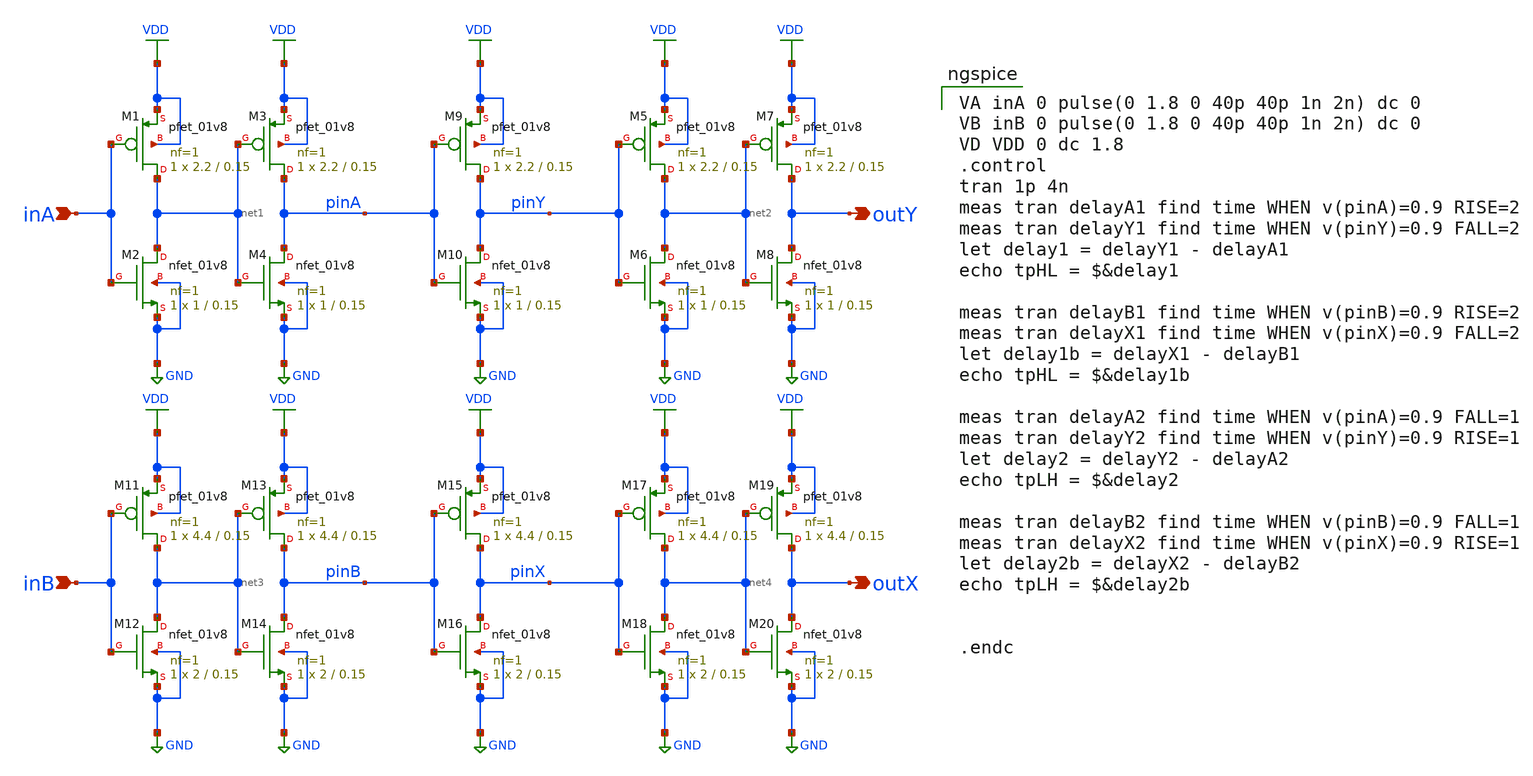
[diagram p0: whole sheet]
** sch_path: inv_delay2.sch
**.subckt inv_delay2 inA outY inB outX
*.ipin inA
*.opin outY
*.ipin inB
*.opin outX
XM1 net1 inA VDD VDD sky130_fd_pr__pfet_01v8 L=0.15 W=2.2 nf=1 ad='int((nf+1)/2) * W/nf * 0.29' as='int((nf+2)/2) * W/nf * 0.29'
+ pd='2*int((nf+1)/2) * (W/nf + 0.29)' ps='2*int((nf+2)/2) * (W/nf + 0.29)' nrd='0.29 / W' nrs='0.29 / W'
+ sa=0 sb=0 sd=0 mult=1 m=1
XM2 net1 inA GND GND sky130_fd_pr__nfet_01v8 L=0.15 W=1 nf=1 ad='int((nf+1)/2) * W/nf * 0.29' as='int((nf+2)/2) * W/nf * 0.29'
+ pd='2*int((nf+1)/2) * (W/nf + 0.29)' ps='2*int((nf+2)/2) * (W/nf + 0.29)' nrd='0.29 / W' nrs='0.29 / W'
+ sa=0 sb=0 sd=0 mult=1 m=1
XM3 pinA net1 VDD VDD sky130_fd_pr__pfet_01v8 L=0.15 W=2.2 nf=1 ad='int((nf+1)/2) * W/nf * 0.29' as='int((nf+2)/2) * W/nf * 0.29'
+ pd='2*int((nf+1)/2) * (W/nf + 0.29)' ps='2*int((nf+2)/2) * (W/nf + 0.29)' nrd='0.29 / W' nrs='0.29 / W'
+ sa=0 sb=0 sd=0 mult=1 m=1
XM4 pinA net1 GND GND sky130_fd_pr__nfet_01v8 L=0.15 W=1 nf=1 ad='int((nf+1)/2) * W/nf * 0.29' as='int((nf+2)/2) * W/nf * 0.29'
+ pd='2*int((nf+1)/2) * (W/nf + 0.29)' ps='2*int((nf+2)/2) * (W/nf + 0.29)' nrd='0.29 / W' nrs='0.29 / W'
+ sa=0 sb=0 sd=0 mult=1 m=1
XM5 net2 pinY VDD VDD sky130_fd_pr__pfet_01v8 L=0.15 W=2.2 nf=1 ad='int((nf+1)/2) * W/nf * 0.29' as='int((nf+2)/2) * W/nf * 0.29'
+ pd='2*int((nf+1)/2) * (W/nf + 0.29)' ps='2*int((nf+2)/2) * (W/nf + 0.29)' nrd='0.29 / W' nrs='0.29 / W'
+ sa=0 sb=0 sd=0 mult=1 m=1
XM6 net2 pinY GND GND sky130_fd_pr__nfet_01v8 L=0.15 W=1 nf=1 ad='int((nf+1)/2) * W/nf * 0.29' as='int((nf+2)/2) * W/nf * 0.29'
+ pd='2*int((nf+1)/2) * (W/nf + 0.29)' ps='2*int((nf+2)/2) * (W/nf + 0.29)' nrd='0.29 / W' nrs='0.29 / W'
+ sa=0 sb=0 sd=0 mult=1 m=1
XM7 outY net2 VDD VDD sky130_fd_pr__pfet_01v8 L=0.15 W=2.2 nf=1 ad='int((nf+1)/2) * W/nf * 0.29' as='int((nf+2)/2) * W/nf * 0.29'
+ pd='2*int((nf+1)/2) * (W/nf + 0.29)' ps='2*int((nf+2)/2) * (W/nf + 0.29)' nrd='0.29 / W' nrs='0.29 / W'
+ sa=0 sb=0 sd=0 mult=1 m=1
XM8 outY net2 GND GND sky130_fd_pr__nfet_01v8 L=0.15 W=1 nf=1 ad='int((nf+1)/2) * W/nf * 0.29' as='int((nf+2)/2) * W/nf * 0.29'
+ pd='2*int((nf+1)/2) * (W/nf + 0.29)' ps='2*int((nf+2)/2) * (W/nf + 0.29)' nrd='0.29 / W' nrs='0.29 / W'
+ sa=0 sb=0 sd=0 mult=1 m=1
XM9 pinY pinA VDD VDD sky130_fd_pr__pfet_01v8 L=0.15 W=2.2 nf=1 ad='int((nf+1)/2) * W/nf * 0.29' as='int((nf+2)/2) * W/nf * 0.29'
+ pd='2*int((nf+1)/2) * (W/nf + 0.29)' ps='2*int((nf+2)/2) * (W/nf + 0.29)' nrd='0.29 / W' nrs='0.29 / W'
+ sa=0 sb=0 sd=0 mult=1 m=1
XM10 pinY pinA GND GND sky130_fd_pr__nfet_01v8 L=0.15 W=1 nf=1 ad='int((nf+1)/2) * W/nf * 0.29' as='int((nf+2)/2) * W/nf * 0.29'
+ pd='2*int((nf+1)/2) * (W/nf + 0.29)' ps='2*int((nf+2)/2) * (W/nf + 0.29)' nrd='0.29 / W' nrs='0.29 / W'
+ sa=0 sb=0 sd=0 mult=1 m=1
XM11 net3 inB VDD VDD sky130_fd_pr__pfet_01v8 L=0.15 W=4.4 nf=1 ad='int((nf+1)/2) * W/nf * 0.29' as='int((nf+2)/2) * W/nf * 0.29'
+ pd='2*int((nf+1)/2) * (W/nf + 0.29)' ps='2*int((nf+2)/2) * (W/nf + 0.29)' nrd='0.29 / W' nrs='0.29 / W'
+ sa=0 sb=0 sd=0 mult=1 m=1
XM12 net3 inB GND GND sky130_fd_pr__nfet_01v8 L=0.15 W=2 nf=1 ad='int((nf+1)/2) * W/nf * 0.29' as='int((nf+2)/2) * W/nf * 0.29'
+ pd='2*int((nf+1)/2) * (W/nf + 0.29)' ps='2*int((nf+2)/2) * (W/nf + 0.29)' nrd='0.29 / W' nrs='0.29 / W'
+ sa=0 sb=0 sd=0 mult=1 m=1
XM19 outX net4 VDD VDD sky130_fd_pr__pfet_01v8 L=0.15 W=4.4 nf=1 ad='int((nf+1)/2) * W/nf * 0.29' as='int((nf+2)/2) * W/nf * 0.29'
+ pd='2*int((nf+1)/2) * (W/nf + 0.29)' ps='2*int((nf+2)/2) * (W/nf + 0.29)' nrd='0.29 / W' nrs='0.29 / W'
+ sa=0 sb=0 sd=0 mult=1 m=1
XM13 pinB net3 VDD VDD sky130_fd_pr__pfet_01v8 L=0.15 W=4.4 nf=1 ad='int((nf+1)/2) * W/nf * 0.29' as='int((nf+2)/2) * W/nf * 0.29'
+ pd='2*int((nf+1)/2) * (W/nf + 0.29)' ps='2*int((nf+2)/2) * (W/nf + 0.29)' nrd='0.29 / W' nrs='0.29 / W'
+ sa=0 sb=0 sd=0 mult=1 m=1
XM15 pinX pinB VDD VDD sky130_fd_pr__pfet_01v8 L=0.15 W=4.4 nf=1 ad='int((nf+1)/2) * W/nf * 0.29' as='int((nf+2)/2) * W/nf * 0.29'
+ pd='2*int((nf+1)/2) * (W/nf + 0.29)' ps='2*int((nf+2)/2) * (W/nf + 0.29)' nrd='0.29 / W' nrs='0.29 / W'
+ sa=0 sb=0 sd=0 mult=1 m=1
XM17 net4 pinX VDD VDD sky130_fd_pr__pfet_01v8 L=0.15 W=4.4 nf=1 ad='int((nf+1)/2) * W/nf * 0.29' as='int((nf+2)/2) * W/nf * 0.29'
+ pd='2*int((nf+1)/2) * (W/nf + 0.29)' ps='2*int((nf+2)/2) * (W/nf + 0.29)' nrd='0.29 / W' nrs='0.29 / W'
+ sa=0 sb=0 sd=0 mult=1 m=1
XM14 pinB net3 GND GND sky130_fd_pr__nfet_01v8 L=0.15 W=2 nf=1 ad='int((nf+1)/2) * W/nf * 0.29' as='int((nf+2)/2) * W/nf * 0.29'
+ pd='2*int((nf+1)/2) * (W/nf + 0.29)' ps='2*int((nf+2)/2) * (W/nf + 0.29)' nrd='0.29 / W' nrs='0.29 / W'
+ sa=0 sb=0 sd=0 mult=1 m=1
XM16 pinX pinB GND GND sky130_fd_pr__nfet_01v8 L=0.15 W=2 nf=1 ad='int((nf+1)/2) * W/nf * 0.29' as='int((nf+2)/2) * W/nf * 0.29'
+ pd='2*int((nf+1)/2) * (W/nf + 0.29)' ps='2*int((nf+2)/2) * (W/nf + 0.29)' nrd='0.29 / W' nrs='0.29 / W'
+ sa=0 sb=0 sd=0 mult=1 m=1
XM18 net4 pinX GND GND sky130_fd_pr__nfet_01v8 L=0.15 W=2 nf=1 ad='int((nf+1)/2) * W/nf * 0.29' as='int((nf+2)/2) * W/nf * 0.29'
+ pd='2*int((nf+1)/2) * (W/nf + 0.29)' ps='2*int((nf+2)/2) * (W/nf + 0.29)' nrd='0.29 / W' nrs='0.29 / W'
+ sa=0 sb=0 sd=0 mult=1 m=1
XM20 outX net4 GND GND sky130_fd_pr__nfet_01v8 L=0.15 W=2 nf=1 ad='int((nf+1)/2) * W/nf * 0.29' as='int((nf+2)/2) * W/nf * 0.29'
+ pd='2*int((nf+1)/2) * (W/nf + 0.29)' ps='2*int((nf+2)/2) * (W/nf + 0.29)' nrd='0.29 / W' nrs='0.29 / W'
+ sa=0 sb=0 sd=0 mult=1 m=1
**** begin user architecture code

VA inA 0 pulse(0 1.8 0 40p 40p 1n 2n) dc 0
VB inB 0 pulse(0 1.8 0 40p 40p 1n 2n) dc 0
VD VDD 0 dc 1.8
.control
tran 1p 4n
meas tran delayA1 find time WHEN v(pinA)=0.9 RISE=2
meas tran delayY1 find time WHEN v(pinY)=0.9 FALL=2
let delay1 = delayY1 - delayA1
echo tpHL = $&delay1

meas tran delayB1 find time WHEN v(pinB)=0.9 RISE=2
meas tran delayX1 find time WHEN v(pinX)=0.9 FALL=2
let delay1b = delayX1 - delayB1
echo tpHL = $&delay1b

meas tran delayA2 find time WHEN v(pinA)=0.9 FALL=1
meas tran delayY2 find time WHEN v(pinY)=0.9 RISE=1
let delay2 = delayY2 - delayA2
echo tpLH = $&delay2

meas tran delayB2 find time WHEN v(pinB)=0.9 FALL=1
meas tran delayX2 find time WHEN v(pinX)=0.9 RISE=1
let delay2b = delayX2 - delayB2
echo tpLH = $&delay2b


.endc

 .param mc_mm_switch=0
.param mc_pr_switch=0
.include $::SKYWATER_MODELS/corners/tt.spice
.include $::SKYWATER_MODELS/r+c/res_typical__cap_typical.spice
.include $::SKYWATER_MODELS/r+c/res_typical__cap_typical__lin.spice
.include $::SKYWATER_MODELS/corners/tt/specialized_cells.spice
.include $::SKYWATER_STDCELLS/sky130_fd_sc_hd.spice

**** end user architecture code
**.ends
.GLOBAL GND
.GLOBAL VDD
.end
